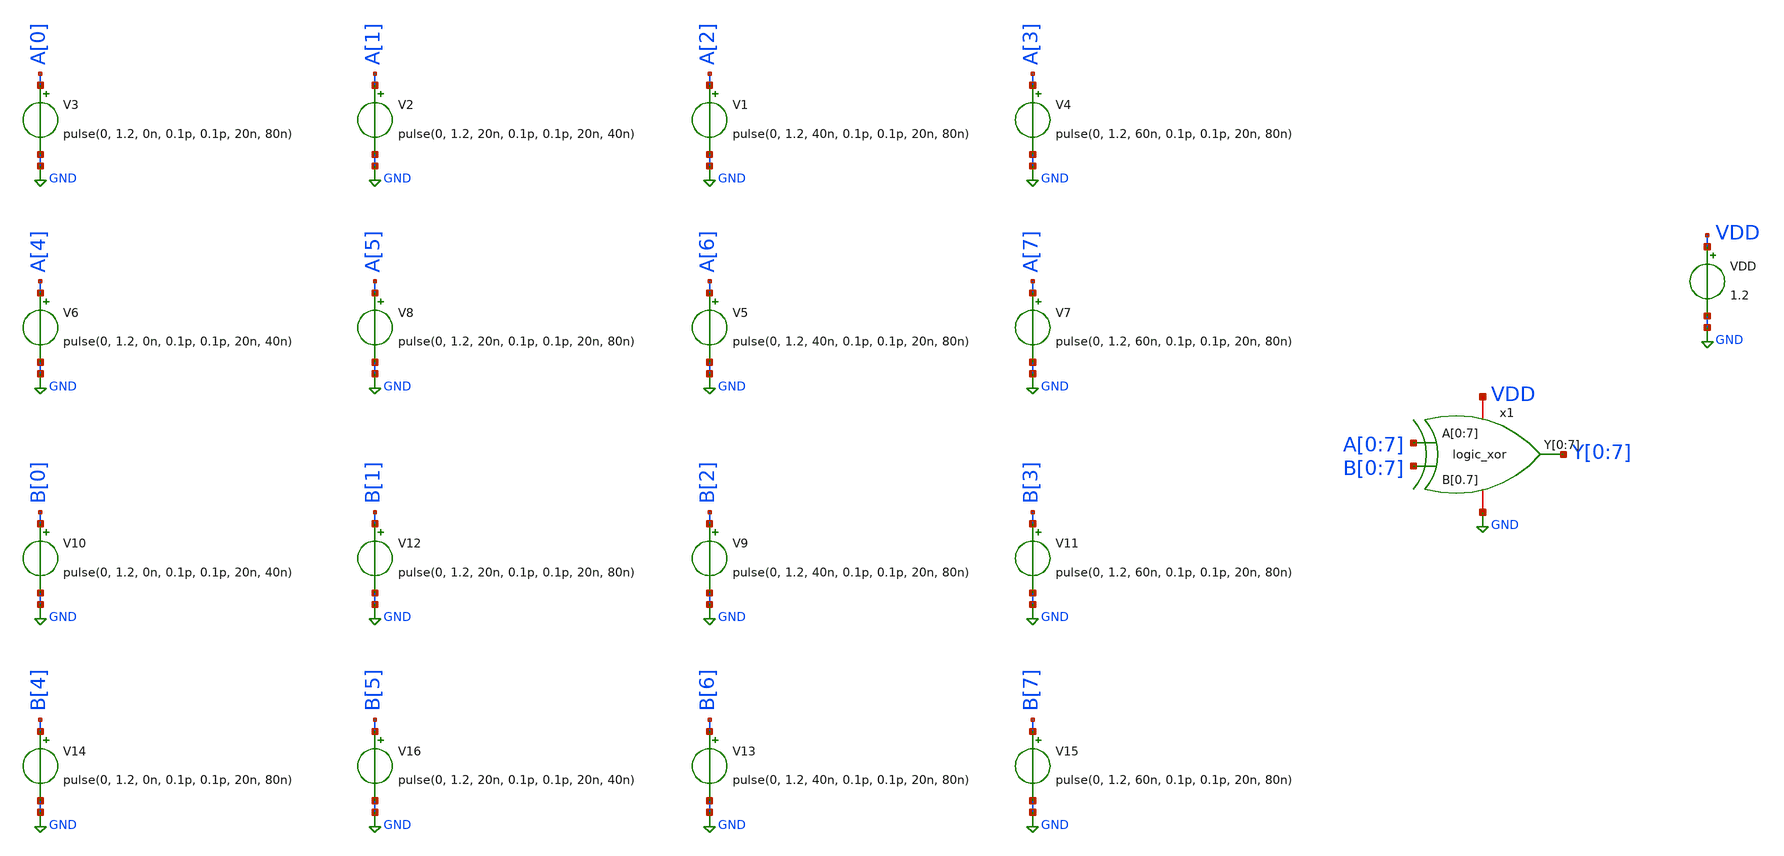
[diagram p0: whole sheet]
** sch_path: design/8_BIT_XOR/xschem/logic_xor_tb.sch
**.subckt logic_xor_tb
VDD VDD GND 1.2
V1 A[2] GND pulse(0, 1.2, 40n, 0.1p, 0.1p, 20n, 80n)
V3 A[0] GND pulse(0, 1.2, 0n, 0.1p, 0.1p, 20n, 80n)
V4 A[3] GND pulse(0, 1.2, 60n, 0.1p, 0.1p, 20n, 80n)
V2 A[1] GND pulse(0, 1.2, 20n, 0.1p, 0.1p, 20n, 40n)
V5 A[6] GND pulse(0, 1.2, 40n, 0.1p, 0.1p, 20n, 80n)
V6 A[4] GND pulse(0, 1.2, 0n, 0.1p, 0.1p, 20n, 40n)
V7 A[7] GND pulse(0, 1.2, 60n, 0.1p, 0.1p, 20n, 80n)
V8 A[5] GND pulse(0, 1.2, 20n, 0.1p, 0.1p, 20n, 80n)
V9 B[2] GND pulse(0, 1.2, 40n, 0.1p, 0.1p, 20n, 80n)
V11 B[3] GND pulse(0, 1.2, 60n, 0.1p, 0.1p, 20n, 80n)
V12 B[1] GND pulse(0, 1.2, 20n, 0.1p, 0.1p, 20n, 80n)
V13 B[6] GND pulse(0, 1.2, 40n, 0.1p, 0.1p, 20n, 80n)
V14 B[4] GND pulse(0, 1.2, 0n, 0.1p, 0.1p, 20n, 80n)
V15 B[7] GND pulse(0, 1.2, 60n, 0.1p, 0.1p, 20n, 80n)
V10 B[0] GND pulse(0, 1.2, 0n, 0.1p, 0.1p, 20n, 40n)
V16 B[5] GND pulse(0, 1.2, 20n, 0.1p, 0.1p, 20n, 40n)
x1 A[0] A[1] A[2] A[3] A[4] A[5] A[6] A[7] Y[0] Y[1] Y[2] Y[3] Y[4] Y[5] Y[6] Y[7] GND VDD B[0] B[1]
+ B[2] B[3] B[4] B[5] B[6] B[7] logic_xor
**** begin user architecture code

** opencircuitdesign pdks install
.lib $::SKYWATER_MODELS/sky130.lib.spice tt_mm



.control
save all

set color0 = white
tran 1p 80n
plot "a[0]" "a[1]"+2 "a[2]"+4 "a[3]"+6 "a[4]"+8 "a[5]"+10 "a[6]"+12 "a[7]"+14
plot "b[0]" "b[1]"+2 "b[2]"+4 "b[3]"+6 "b[4]"+8 "b[5]"+10 "b[6]"+12 "b[7]"+14
plot "y[0]" "y[1]"+2 "y[2]"+4 "y[3]"+6 "y[4]"+8 "y[5]"+10 "y[6]"+12 "y[7]"+14
.endc

**** end user architecture code
**.ends
.GLOBAL GND
.end
